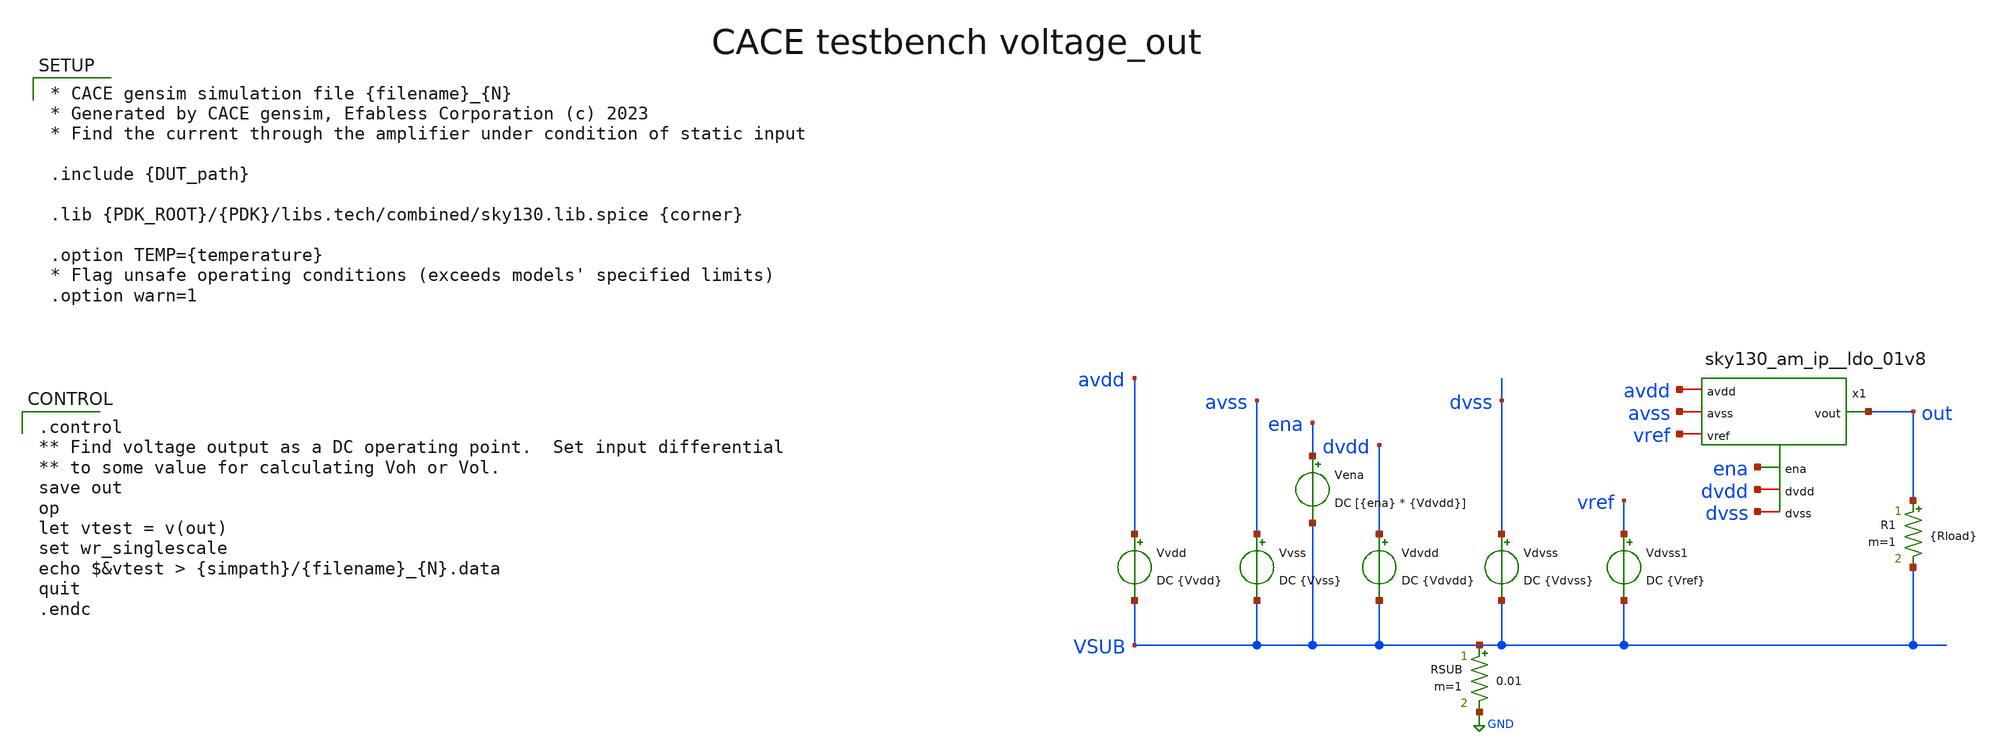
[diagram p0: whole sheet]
** sch_path: cace/voltage_out.sch
**.subckt voltage_out
Vena ena VSUB DC [{ena} * {Vdvdd}]
Vvss avss VSUB DC {Vvss}
Vvdd avdd VSUB DC {Vvdd}
RSUB VSUB GND 0.01 m=1
Vdvdd dvdd VSUB DC {Vdvdd}
Vdvss dvss VSUB DC {Vdvss}
x1 avdd dvdd ena out avss dvss vref sky130_am_ip__ldo_01v8
R1 out VSUB {Rload} m=1
Vdvss1 vref VSUB DC {Vref}
**** begin user architecture code

.control
** Find voltage output as a DC operating point.  Set input differential
** to some value for calculating Voh or Vol.
save out
op
let vtest = v(out)
set wr_singlescale
echo $&vtest > {simpath}/{filename}_{N}.data
quit
.endc



* CACE gensim simulation file {filename}_{N}
* Generated by CACE gensim, Efabless Corporation (c) 2023
* Find the current through the amplifier under condition of static input

.include {DUT_path}

.lib {PDK_ROOT}/{PDK}/libs.tech/combined/sky130.lib.spice {corner}

.option TEMP={temperature}
* Flag unsafe operating conditions (exceeds models' specified limits)
.option warn=1


**** end user architecture code
**.ends

* expanding   symbol:  sky130_am_ip__ldo_01v8.sym # of pins=7
** sym_path: xschem/sky130_am_ip__ldo_01v8.sym
** sch_path: xschem/sky130_am_ip__ldo_01v8.sch
.subckt sky130_am_ip__ldo_01v8 avdd dvdd ena vout avss dvss vref
*.opin vout
*.iopin dvdd
*.iopin dvss
*.ipin vref
*.ipin ena
*.iopin avdd
*.iopin avss
XM11 avdd v_ea vout avss sky130_fd_pr__nfet_g5v0d10v5 L=1 W=200 nf=1 ad='int((nf+1)/2) * W/nf * 0.29' as='int((nf+2)/2)
+ * W/nf * 0.29' pd='2*int((nf+1)/2) * (W/nf + 0.29)' ps='2*int((nf+2)/2) * (W/nf + 0.29)' nrd='0.29 /
+ W' nrs='0.29 / W' sa=0 sb=0 sd=0 mult=1 m=1
XR1 v_m vout avss sky130_fd_pr__res_high_po_0p35 L=1000 mult=1 m=1
XR2 avss v_m avss sky130_fd_pr__res_high_po_0p35 L=2000 mult=1 m=1
XM10 vi vi avdd avdd sky130_fd_pr__pfet_g5v0d10v5 L=20 W=1 nf=1 ad='int((nf+1)/2) * W/nf * 0.29' as='int((nf+2)/2)
+ * W/nf * 0.29' pd='2*int((nf+1)/2) * (W/nf + 0.29)' ps='2*int((nf+2)/2) * (W/nf + 0.29)' nrd='0.29 /
+ W' nrs='0.29 / W' sa=0 sb=0 sd=0 mult=1 m=1
XM16 vi vi avss avss sky130_fd_pr__nfet_g5v0d10v5 L=20 W=2.5 nf=1 ad='int((nf+1)/2) * W/nf * 0.29' as='int((nf+2)/2)
+ * W/nf * 0.29' pd='2*int((nf+1)/2) * (W/nf + 0.29)' ps='2*int((nf+2)/2) * (W/nf + 0.29)' nrd='0.29 /
+ W' nrs='0.29 / W' sa=0 sb=0 sd=0 mult=1 m=1
x1 ena dvdd v_ea v_m vref dvss avdd avss error_amplifier
.ends


* expanding   symbol:  error_amplifier.sym # of pins=8
** sym_path: xschem/error_amplifier.sym
** sch_path: xschem/error_amplifier.sch
.subckt error_amplifier ena dvdd out in_m in_p dvss avdd avss
*.iopin avdd
*.iopin avss
*.ipin in_m
*.ipin in_p
*.opin out
*.ipin ena
*.iopin dvdd
*.iopin dvss
XM1 vbn vbn avss avss sky130_fd_pr__nfet_g5v0d10v5 L=10 W=1 nf=1 ad='int((nf+1)/2) * W/nf * 0.29' as='int((nf+2)/2)
+ * W/nf * 0.29' pd='2*int((nf+1)/2) * (W/nf + 0.29)' ps='2*int((nf+2)/2) * (W/nf + 0.29)' nrd='0.29 /
+ W' nrs='0.29 / W' sa=0 sb=0 sd=0 mult=1 m=1
XM3 vcp vbn net6 avss sky130_fd_pr__nfet_g5v0d10v5 L=10 W=1 nf=1 ad='int((nf+1)/2) * W/nf * 0.29' as='int((nf+2)/2)
+ * W/nf * 0.29' pd='2*int((nf+1)/2) * (W/nf + 0.29)' ps='2*int((nf+2)/2) * (W/nf + 0.29)' nrd='0.29 /
+ W' nrs='0.29 / W' sa=0 sb=0 sd=0 mult=4 m=4
XM5 vbp vbp avdd avdd sky130_fd_pr__pfet_g5v0d10v5 L=10 W=1 nf=1 ad='int((nf+1)/2) * W/nf * 0.29' as='int((nf+2)/2)
+ * W/nf * 0.29' pd='2*int((nf+1)/2) * (W/nf + 0.29)' ps='2*int((nf+2)/2) * (W/nf + 0.29)' nrd='0.29 /
+ W' nrs='0.29 / W' sa=0 sb=0 sd=0 mult=2 m=2
XM26 net4 vbp avdd avdd sky130_fd_pr__pfet_g5v0d10v5 L=10 W=1 nf=1 ad='int((nf+1)/2) * W/nf * 0.29' as='int((nf+2)/2)
+ * W/nf * 0.29' pd='2*int((nf+1)/2) * (W/nf + 0.29)' ps='2*int((nf+2)/2) * (W/nf + 0.29)' nrd='0.29 /
+ W' nrs='0.29 / W' sa=0 sb=0 sd=0 mult=6 m=6
XM27 net5 vbp avdd avdd sky130_fd_pr__pfet_g5v0d10v5 L=10 W=1 nf=1 ad='int((nf+1)/2) * W/nf * 0.29' as='int((nf+2)/2)
+ * W/nf * 0.29' pd='2*int((nf+1)/2) * (W/nf + 0.29)' ps='2*int((nf+2)/2) * (W/nf + 0.29)' nrd='0.29 /
+ W' nrs='0.29 / W' sa=0 sb=0 sd=0 mult=6 m=6
XM28 net3 vcp net4 avdd sky130_fd_pr__pfet_g5v0d10v5 L=2 W=1 nf=1 ad='int((nf+1)/2) * W/nf * 0.29' as='int((nf+2)/2)
+ * W/nf * 0.29' pd='2*int((nf+1)/2) * (W/nf + 0.29)' ps='2*int((nf+2)/2) * (W/nf + 0.29)' nrd='0.29 /
+ W' nrs='0.29 / W' sa=0 sb=0 sd=0 mult=1 m=1
XM29 v_cascode vcp net5 avdd sky130_fd_pr__pfet_g5v0d10v5 L=2 W=1 nf=1 ad='int((nf+1)/2) * W/nf * 0.29' as='int((nf+2)/2)
+ * W/nf * 0.29' pd='2*int((nf+1)/2) * (W/nf + 0.29)' ps='2*int((nf+2)/2) * (W/nf + 0.29)' nrd='0.29 /
+ W' nrs='0.29 / W' sa=0 sb=0 sd=0 mult=1 m=1
XM30 net3 vcn net1 avss sky130_fd_pr__nfet_g5v0d10v5 L=2 W=1 nf=1 ad='int((nf+1)/2) * W/nf * 0.29' as='int((nf+2)/2)
+ * W/nf * 0.29' pd='2*int((nf+1)/2) * (W/nf + 0.29)' ps='2*int((nf+2)/2) * (W/nf + 0.29)' nrd='0.29 /
+ W' nrs='0.29 / W' sa=0 sb=0 sd=0 mult=1 m=1
XM31 v_cascode vcn net2 avss sky130_fd_pr__nfet_g5v0d10v5 L=2 W=1 nf=1 ad='int((nf+1)/2) * W/nf * 0.29' as='int((nf+2)/2)
+ * W/nf * 0.29' pd='2*int((nf+1)/2) * (W/nf + 0.29)' ps='2*int((nf+2)/2) * (W/nf + 0.29)' nrd='0.29 /
+ W' nrs='0.29 / W' sa=0 sb=0 sd=0 mult=1 m=1
XM32 net1 net3 avss avss sky130_fd_pr__nfet_g5v0d10v5 L=10 W=1 nf=1 ad='int((nf+1)/2) * W/nf * 0.29' as='int((nf+2)/2)
+ * W/nf * 0.29' pd='2*int((nf+1)/2) * (W/nf + 0.29)' ps='2*int((nf+2)/2) * (W/nf + 0.29)' nrd='0.29 /
+ W' nrs='0.29 / W' sa=0 sb=0 sd=0 mult=3 m=3
XM33 net2 net3 avss avss sky130_fd_pr__nfet_g5v0d10v5 L=10 W=1 nf=1 ad='int((nf+1)/2) * W/nf * 0.29' as='int((nf+2)/2)
+ * W/nf * 0.29' pd='2*int((nf+1)/2) * (W/nf + 0.29)' ps='2*int((nf+2)/2) * (W/nf + 0.29)' nrd='0.29 /
+ W' nrs='0.29 / W' sa=0 sb=0 sd=0 mult=3 m=3
XM35 net11 vbp avdd avdd sky130_fd_pr__pfet_g5v0d10v5 L=10 W=1 nf=1 ad='int((nf+1)/2) * W/nf * 0.29' as='int((nf+2)/2)
+ * W/nf * 0.29' pd='2*int((nf+1)/2) * (W/nf + 0.29)' ps='2*int((nf+2)/2) * (W/nf + 0.29)' nrd='0.29 /
+ W' nrs='0.29 / W' sa=0 sb=0 sd=0 mult=2 m=2
XR3 avss net6 avss sky130_fd_pr__res_xhigh_po_0p35 L=180 mult=1 m=1
XM9 net13 v_cascode out avdd sky130_fd_pr__pfet_g5v0d10v5 L=10 W=1 nf=1 ad='int((nf+1)/2) * W/nf * 0.29' as='int((nf+2)/2)
+ * W/nf * 0.29' pd='2*int((nf+1)/2) * (W/nf + 0.29)' ps='2*int((nf+2)/2) * (W/nf + 0.29)' nrd='0.29 /
+ W' nrs='0.29 / W' sa=0 sb=0 sd=0 mult=1 m=1
XM8 out vbp avdd avdd sky130_fd_pr__pfet_g5v0d10v5 L=10 W=1 nf=1 ad='int((nf+1)/2) * W/nf * 0.29' as='int((nf+2)/2)
+ * W/nf * 0.29' pd='2*int((nf+1)/2) * (W/nf + 0.29)' ps='2*int((nf+2)/2) * (W/nf + 0.29)' nrd='0.29 /
+ W' nrs='0.29 / W' sa=0 sb=0 sd=0 mult=10 m=10
XM17 net8 vbp avdd avdd sky130_fd_pr__pfet_g5v0d10v5 L=10 W=1 nf=1 ad='int((nf+1)/2) * W/nf * 0.29' as='int((nf+2)/2)
+ * W/nf * 0.29' pd='2*int((nf+1)/2) * (W/nf + 0.29)' ps='2*int((nf+2)/2) * (W/nf + 0.29)' nrd='0.29 /
+ W' nrs='0.29 / W' sa=0 sb=0 sd=0 mult=1 m=1
XM19 net8 net8 net7 avss sky130_fd_pr__nfet_g5v0d10v5 L=0.5 W=1 nf=1 ad='int((nf+1)/2) * W/nf * 0.29' as='int((nf+2)/2)
+ * W/nf * 0.29' pd='2*int((nf+1)/2) * (W/nf + 0.29)' ps='2*int((nf+2)/2) * (W/nf + 0.29)' nrd='0.29 /
+ W' nrs='0.29 / W' sa=0 sb=0 sd=0 mult=6 m=6
XM20 net7 net8 avss avss sky130_fd_pr__nfet_g5v0d10v5 L=0.5 W=1 nf=1 ad='int((nf+1)/2) * W/nf * 0.29' as='int((nf+2)/2)
+ * W/nf * 0.29' pd='2*int((nf+1)/2) * (W/nf + 0.29)' ps='2*int((nf+2)/2) * (W/nf + 0.29)' nrd='0.29 /
+ W' nrs='0.29 / W' sa=0 sb=0 sd=0 mult=1 m=1
XM21 vcn vbp avdd avdd sky130_fd_pr__pfet_g5v0d10v5 L=10 W=1 nf=1 ad='int((nf+1)/2) * W/nf * 0.29' as='int((nf+2)/2)
+ * W/nf * 0.29' pd='2*int((nf+1)/2) * (W/nf + 0.29)' ps='2*int((nf+2)/2) * (W/nf + 0.29)' nrd='0.29 /
+ W' nrs='0.29 / W' sa=0 sb=0 sd=0 mult=5 m=5
XM36 vcn vcn net7 avss sky130_fd_pr__nfet_g5v0d10v5 L=2 W=1 nf=1 ad='int((nf+1)/2) * W/nf * 0.29' as='int((nf+2)/2)
+ * W/nf * 0.29' pd='2*int((nf+1)/2) * (W/nf + 0.29)' ps='2*int((nf+2)/2) * (W/nf + 0.29)' nrd='0.29 /
+ W' nrs='0.29 / W' sa=0 sb=0 sd=0 mult=1 m=1
XM6 net5 in_m net9 avss sky130_fd_pr__nfet_g5v0d10v5 L=0.5 W=1 nf=1 ad='int((nf+1)/2) * W/nf * 0.29' as='int((nf+2)/2)
+ * W/nf * 0.29' pd='2*int((nf+1)/2) * (W/nf + 0.29)' ps='2*int((nf+2)/2) * (W/nf + 0.29)' nrd='0.29 /
+ W' nrs='0.29 / W' sa=0 sb=0 sd=0 mult=1 m=1
XM7 net9 vbn avss avss sky130_fd_pr__nfet_g5v0d10v5 L=10 W=1 nf=1 ad='int((nf+1)/2) * W/nf * 0.29' as='int((nf+2)/2)
+ * W/nf * 0.29' pd='2*int((nf+1)/2) * (W/nf + 0.29)' ps='2*int((nf+2)/2) * (W/nf + 0.29)' nrd='0.29 /
+ W' nrs='0.29 / W' sa=0 sb=0 sd=0 mult=2 m=2
XM12 net4 in_p net9 avss sky130_fd_pr__nfet_g5v0d10v5 L=0.5 W=1 nf=1 ad='int((nf+1)/2) * W/nf * 0.29' as='int((nf+2)/2)
+ * W/nf * 0.29' pd='2*int((nf+1)/2) * (W/nf + 0.29)' ps='2*int((nf+2)/2) * (W/nf + 0.29)' nrd='0.29 /
+ W' nrs='0.29 / W' sa=0 sb=0 sd=0 mult=1 m=1
XM10 vstart vbn avss avss sky130_fd_pr__nfet_g5v0d10v5 L=1 W=10 nf=1 ad='int((nf+1)/2) * W/nf * 0.29' as='int((nf+2)/2)
+ * W/nf * 0.29' pd='2*int((nf+1)/2) * (W/nf + 0.29)' ps='2*int((nf+2)/2) * (W/nf + 0.29)' nrd='0.29 /
+ W' nrs='0.29 / W' sa=0 sb=0 sd=0 mult=1 m=1
XM11 vstart avss net10 avdd sky130_fd_pr__pfet_g5v0d10v5 L=20 W=1 nf=1 ad='int((nf+1)/2) * W/nf * 0.29' as='int((nf+2)/2)
+ * W/nf * 0.29' pd='2*int((nf+1)/2) * (W/nf + 0.29)' ps='2*int((nf+2)/2) * (W/nf + 0.29)' nrd='0.29 /
+ W' nrs='0.29 / W' sa=0 sb=0 sd=0 mult=1 m=1
XM2 vcp vcp vbp avdd sky130_fd_pr__pfet_g5v0d10v5 L=10 W=1 nf=1 ad='int((nf+1)/2) * W/nf * 0.29' as='int((nf+2)/2)
+ * W/nf * 0.29' pd='2*int((nf+1)/2) * (W/nf + 0.29)' ps='2*int((nf+2)/2) * (W/nf + 0.29)' nrd='0.29 /
+ W' nrs='0.29 / W' sa=0 sb=0 sd=0 mult=2 m=2
XM4 vbn vcp net11 avdd sky130_fd_pr__pfet_g5v0d10v5 L=10 W=1 nf=1 ad='int((nf+1)/2) * W/nf * 0.29' as='int((nf+2)/2)
+ * W/nf * 0.29' pd='2*int((nf+1)/2) * (W/nf + 0.29)' ps='2*int((nf+2)/2) * (W/nf + 0.29)' nrd='0.29 /
+ W' nrs='0.29 / W' sa=0 sb=0 sd=0 mult=2 m=2
XM13 vbp vstart avss avss sky130_fd_pr__nfet_g5v0d10v5 L=0.5 W=1 nf=1 ad='int((nf+1)/2) * W/nf * 0.29' as='int((nf+2)/2)
+ * W/nf * 0.29' pd='2*int((nf+1)/2) * (W/nf + 0.29)' ps='2*int((nf+2)/2) * (W/nf + 0.29)' nrd='0.29 /
+ W' nrs='0.29 / W' sa=0 sb=0 sd=0 mult=1 m=1
XM14 vcp vstart avss avss sky130_fd_pr__nfet_g5v0d10v5 L=0.5 W=1 nf=1 ad='int((nf+1)/2) * W/nf * 0.29' as='int((nf+2)/2)
+ * W/nf * 0.29' pd='2*int((nf+1)/2) * (W/nf + 0.29)' ps='2*int((nf+2)/2) * (W/nf + 0.29)' nrd='0.29 /
+ W' nrs='0.29 / W' sa=0 sb=0 sd=0 mult=1 m=1
XM15 net10 net10 net12 avdd sky130_fd_pr__pfet_g5v0d10v5 L=20 W=1 nf=1 ad='int((nf+1)/2) * W/nf * 0.29' as='int((nf+2)/2)
+ * W/nf * 0.29' pd='2*int((nf+1)/2) * (W/nf + 0.29)' ps='2*int((nf+2)/2) * (W/nf + 0.29)' nrd='0.29 /
+ W' nrs='0.29 / W' sa=0 sb=0 sd=0 mult=1 m=1
XM16 vbp v_ena avdd avdd sky130_fd_pr__pfet_g5v0d10v5 L=0.5 W=1 nf=1 ad='int((nf+1)/2) * W/nf * 0.29' as='int((nf+2)/2)
+ * W/nf * 0.29' pd='2*int((nf+1)/2) * (W/nf + 0.29)' ps='2*int((nf+2)/2) * (W/nf + 0.29)' nrd='0.29 /
+ W' nrs='0.29 / W' sa=0 sb=0 sd=0 mult=1 m=1
XM18 vcp v_ena avdd avdd sky130_fd_pr__pfet_g5v0d10v5 L=0.5 W=1 nf=1 ad='int((nf+1)/2) * W/nf * 0.29' as='int((nf+2)/2)
+ * W/nf * 0.29' pd='2*int((nf+1)/2) * (W/nf + 0.29)' ps='2*int((nf+2)/2) * (W/nf + 0.29)' nrd='0.29 /
+ W' nrs='0.29 / W' sa=0 sb=0 sd=0 mult=1 m=1
XM22 vbn v_ena_b avss avss sky130_fd_pr__nfet_g5v0d10v5 L=0.5 W=1 nf=1 ad='int((nf+1)/2) * W/nf * 0.29' as='int((nf+2)/2)
+ * W/nf * 0.29' pd='2*int((nf+1)/2) * (W/nf + 0.29)' ps='2*int((nf+2)/2) * (W/nf + 0.29)' nrd='0.29 /
+ W' nrs='0.29 / W' sa=0 sb=0 sd=0 mult=1 m=1
XM23 vcn v_ena_b avss avss sky130_fd_pr__nfet_g5v0d10v5 L=0.5 W=1 nf=1 ad='int((nf+1)/2) * W/nf * 0.29' as='int((nf+2)/2)
+ * W/nf * 0.29' pd='2*int((nf+1)/2) * (W/nf + 0.29)' ps='2*int((nf+2)/2) * (W/nf + 0.29)' nrd='0.29 /
+ W' nrs='0.29 / W' sa=0 sb=0 sd=0 mult=1 m=1
XM24 v_cascode v_ena_b avss avss sky130_fd_pr__nfet_g5v0d10v5 L=0.5 W=1 nf=1 ad='int((nf+1)/2) * W/nf
+ * 0.29' as='int((nf+2)/2) * W/nf * 0.29' pd='2*int((nf+1)/2) * (W/nf + 0.29)' ps='2*int((nf+2)/2) * (W/nf
+ + 0.29)' nrd='0.29 / W' nrs='0.29 / W' sa=0 sb=0 sd=0 mult=1 m=1
XM25 out v_ena_b avss avss sky130_fd_pr__nfet_g5v0d10v5 L=0.5 W=1 nf=1 ad='int((nf+1)/2) * W/nf * 0.29' as='int((nf+2)/2)
+ * W/nf * 0.29' pd='2*int((nf+1)/2) * (W/nf + 0.29)' ps='2*int((nf+2)/2) * (W/nf + 0.29)' nrd='0.29 /
+ W' nrs='0.29 / W' sa=0 sb=0 sd=0 mult=1 m=1
XM34 vstart v_ena_b avss avss sky130_fd_pr__nfet_g5v0d10v5 L=0.5 W=1 nf=1 ad='int((nf+1)/2) * W/nf *
+ 0.29' as='int((nf+2)/2) * W/nf * 0.29' pd='2*int((nf+1)/2) * (W/nf + 0.29)' ps='2*int((nf+2)/2) * (W/nf
+ + 0.29)' nrd='0.29 / W' nrs='0.29 / W' sa=0 sb=0 sd=0 mult=1 m=1
XM37 net12 v_ena_b avdd avdd sky130_fd_pr__pfet_g5v0d10v5 L=0.5 W=1 nf=1 ad='int((nf+1)/2) * W/nf * 0.29' as='int((nf+2)/2)
+ * W/nf * 0.29' pd='2*int((nf+1)/2) * (W/nf + 0.29)' ps='2*int((nf+2)/2) * (W/nf + 0.29)' nrd='0.29 /
+ W' nrs='0.29 / W' sa=0 sb=0 sd=0 mult=1 m=1
XM38 net13 vbn avss avss sky130_fd_pr__nfet_g5v0d10v5 L=10 W=1 nf=1 ad='int((nf+1)/2) * W/nf * 0.29' as='int((nf+2)/2)
+ * W/nf * 0.29' pd='2*int((nf+1)/2) * (W/nf + 0.29)' ps='2*int((nf+2)/2) * (W/nf + 0.29)' nrd='0.29 /
+ W' nrs='0.29 / W' sa=0 sb=0 sd=0 mult=2 m=2
XM39 out net13 avss avss sky130_fd_pr__nfet_g5v0d10v5 L=0.5 W=4 nf=1 ad='int((nf+1)/2) * W/nf * 0.29' as='int((nf+2)/2)
+ * W/nf * 0.29' pd='2*int((nf+1)/2) * (W/nf + 0.29)' ps='2*int((nf+2)/2) * (W/nf + 0.29)' nrd='0.29 /
+ W' nrs='0.29 / W' sa=0 sb=0 sd=0 mult=1 m=1
XM41 ena_b ena dvdd dvdd sky130_fd_pr__pfet_g5v0d10v5 L=0.5 W=2.5 nf=1 ad='int((nf+1)/2) * W/nf * 0.29' as='int((nf+2)/2)
+ * W/nf * 0.29' pd='2*int((nf+1)/2) * (W/nf + 0.29)' ps='2*int((nf+2)/2) * (W/nf + 0.29)' nrd='0.29 /
+ W' nrs='0.29 / W' sa=0 sb=0 sd=0 mult=1 m=1
XM42 ena_b ena dvss dvss sky130_fd_pr__nfet_g5v0d10v5 L=0.5 W=1 nf=1 ad='int((nf+1)/2) * W/nf * 0.29' as='int((nf+2)/2)
+ * W/nf * 0.29' pd='2*int((nf+1)/2) * (W/nf + 0.29)' ps='2*int((nf+2)/2) * (W/nf + 0.29)' nrd='0.29 /
+ W' nrs='0.29 / W' sa=0 sb=0 sd=0 mult=1 m=1
XM43 v_ena v_ena_b avdd avdd sky130_fd_pr__pfet_g5v0d10v5 L=0.5 W=2.5 nf=1 ad='int((nf+1)/2) * W/nf *
+ 0.29' as='int((nf+2)/2) * W/nf * 0.29' pd='2*int((nf+1)/2) * (W/nf + 0.29)' ps='2*int((nf+2)/2) * (W/nf
+ + 0.29)' nrd='0.29 / W' nrs='0.29 / W' sa=0 sb=0 sd=0 mult=1 m=1
XM44 v_ena ena_b avss avss sky130_fd_pr__nfet_g5v0d10v5 L=0.5 W=1 nf=1 ad='int((nf+1)/2) * W/nf * 0.29' as='int((nf+2)/2)
+ * W/nf * 0.29' pd='2*int((nf+1)/2) * (W/nf + 0.29)' ps='2*int((nf+2)/2) * (W/nf + 0.29)' nrd='0.29 /
+ W' nrs='0.29 / W' sa=0 sb=0 sd=0 mult=1 m=1
XM45 v_ena_b v_ena avdd avdd sky130_fd_pr__pfet_g5v0d10v5 L=0.5 W=2.5 nf=1 ad='int((nf+1)/2) * W/nf *
+ 0.29' as='int((nf+2)/2) * W/nf * 0.29' pd='2*int((nf+1)/2) * (W/nf + 0.29)' ps='2*int((nf+2)/2) * (W/nf
+ + 0.29)' nrd='0.29 / W' nrs='0.29 / W' sa=0 sb=0 sd=0 mult=1 m=1
XM46 v_ena_b ena avss avss sky130_fd_pr__nfet_g5v0d10v5 L=0.5 W=1 nf=1 ad='int((nf+1)/2) * W/nf * 0.29' as='int((nf+2)/2)
+ * W/nf * 0.29' pd='2*int((nf+1)/2) * (W/nf + 0.29)' ps='2*int((nf+2)/2) * (W/nf + 0.29)' nrd='0.29 /
+ W' nrs='0.29 / W' sa=0 sb=0 sd=0 mult=1 m=1
XC1 out v_cascode sky130_fd_pr__cap_mim_m3_1 W=6 L=6 MF=4 m=4
.ends

.GLOBAL GND
.end
